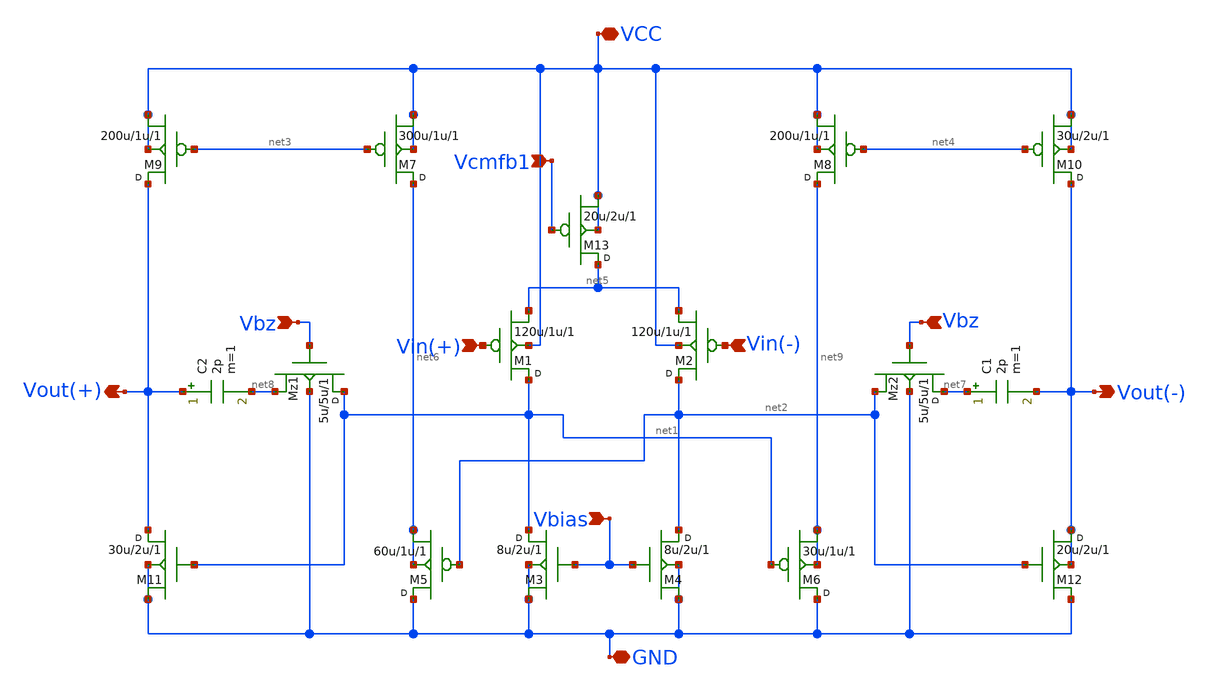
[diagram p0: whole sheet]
** sch_path: blocks/01_OTA/xschem/OTA.sch
**.subckt OTA VCC GND Vout(+) Vout(-) Vin(+) Vin(-) Vcmfb1 Vbias Vbz Vbz
*.iopin VCC
*.iopin GND
*.opin Vout(+)
*.opin Vout(-)
*.ipin Vin(+)
*.ipin Vin(-)
*.ipin Vcmfb1
*.ipin Vbias
*.ipin Vbz
*.ipin Vbz
M1 net1 Vin(+) net5 VCC pmos w=120u l=1u m=1
M2 net2 Vin(-) net5 VCC pmos w=120u l=1u m=1
M3 net1 Vbias GND GND nmos w=8u l=2u m=1
M4 net2 Vbias GND GND nmos w=8u l=2u m=1
M5 GND net2 net6 net6 pmos w=60u l=1u m=1
M6 GND net1 net9 net9 pmos w=30u l=1u m=1
M7 net6 net3 VCC VCC pmos w=300u l=1u m=1
M8 net9 net4 VCC VCC pmos w=200u l=1u m=1
M9 Vout(+) net3 VCC VCC pmos w=200u l=1u m=1
M10 Vout(-) net4 VCC VCC pmos w=30u l=2u m=1
M11 Vout(+) net1 GND GND nmos w=30u l=2u m=1
M12 Vout(-) net2 GND Vout(-) nmos w=20u l=2u m=1
M13 net5 Vcmfb1 VCC VCC pmos w=20u l=2u m=1
Mz1 net1 Vbz net8 GND nmos w=5u l=5u m=1
Mz2 net7 Vbz net2 GND nmos w=5u l=5u m=1
C1 net7 Vout(-) 2p m=1
C2 Vout(+) net8 2p m=1
**.ends
.end
